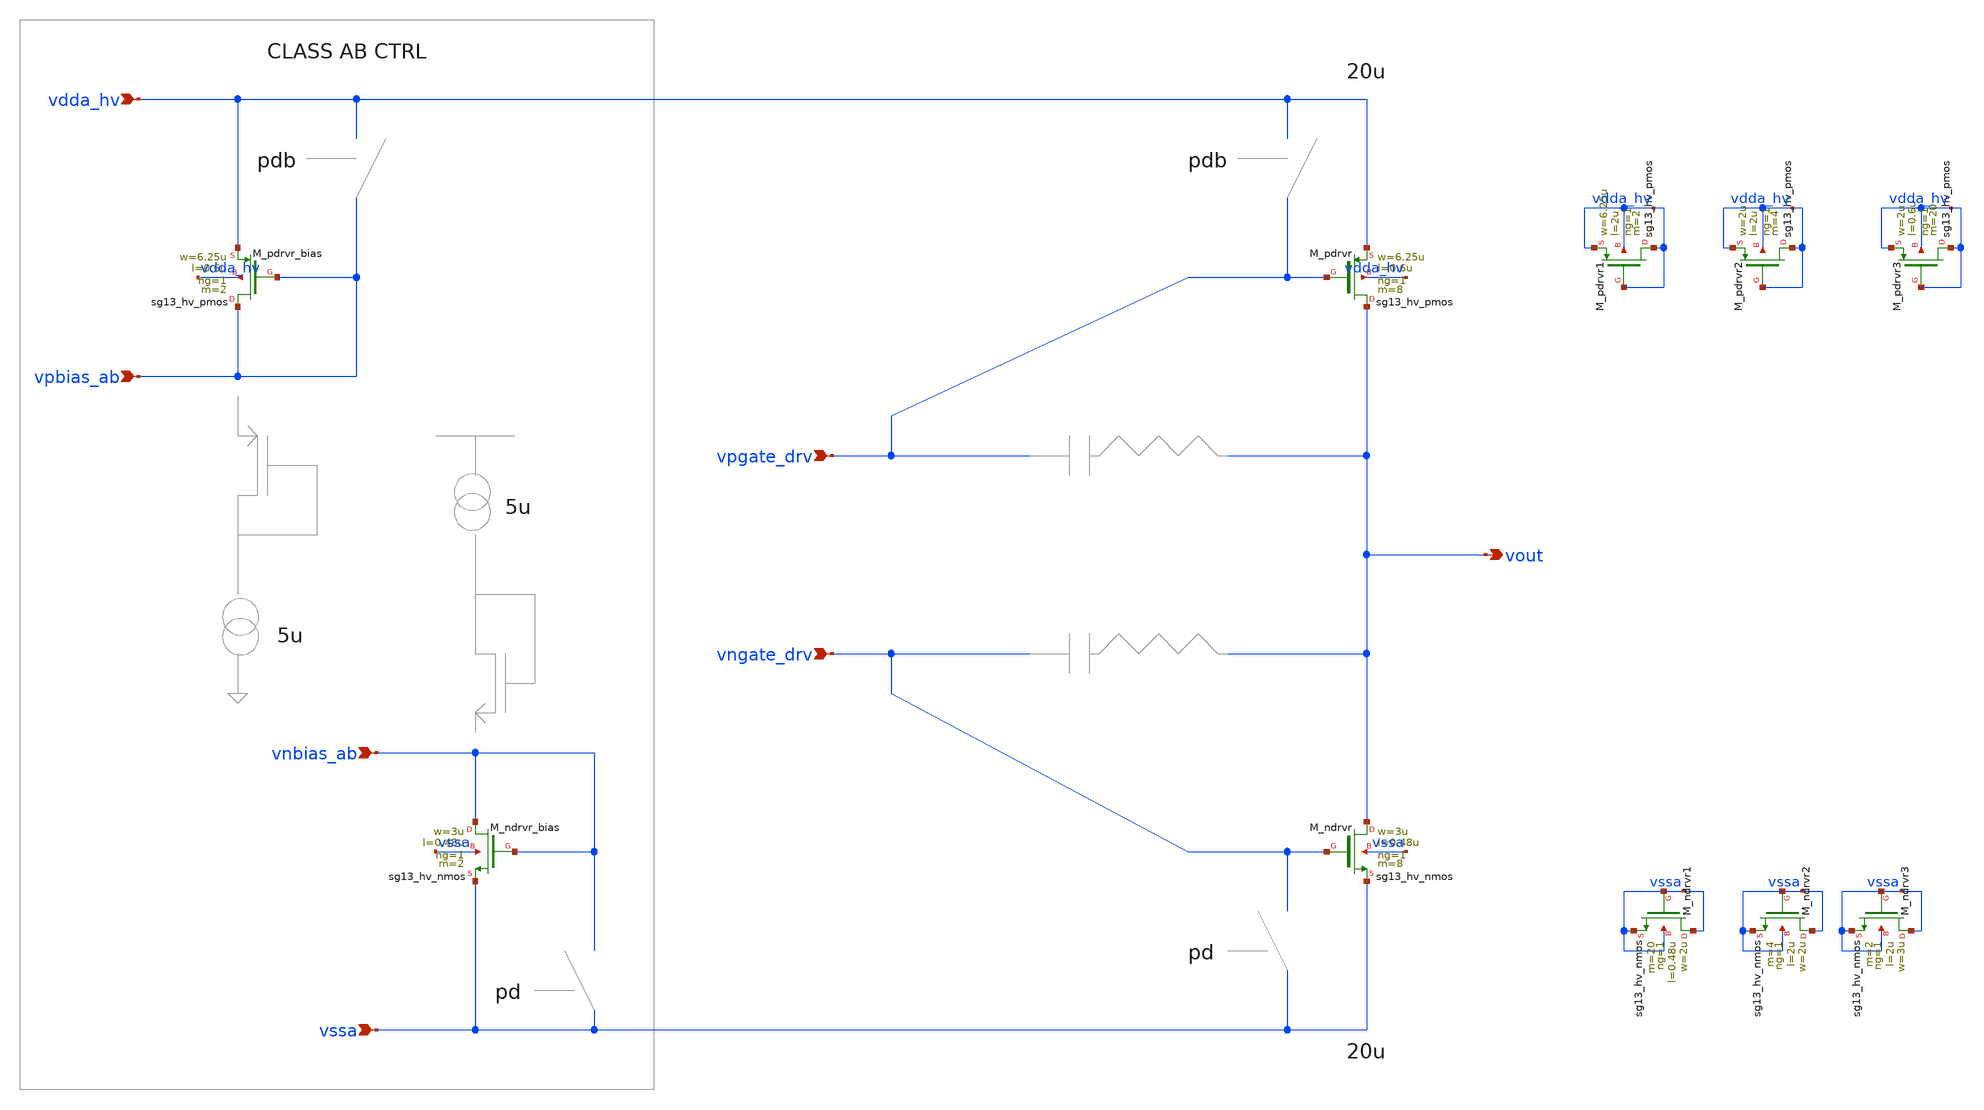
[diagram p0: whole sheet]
** sch_path: Schematics_Layout/sunrise_opamp_stg2_ncomp/sunrise_opamp_stg2_ncomp.sch
**.subckt sunrise_opamp_stg2_ncomp vdda_hv vssa vpgate_drv vngate_drv vout vnbias_ab vpbias_ab
*.ipin vdda_hv
*.ipin vssa
*.ipin vpgate_drv
*.ipin vngate_drv
*.opin vout
*.ipin vnbias_ab
*.ipin vpbias_ab
XM_ndrvr vout vngate_drv vssa vssa sg13_hv_nmos w=3u l=0.48u ng=1 m=8 mm_ok=1
XM_pdrvr vout vpgate_drv vdda_hv vdda_hv sg13_hv_pmos w=6.25u l=0.6u ng=1 m=8 mm_ok=1
XM_pdrvr_bias vpbias_ab vpbias_ab vdda_hv vdda_hv sg13_hv_pmos w=6.25u l=0.6u ng=1 m=2 mm_ok=1
XM_ndrvr_bias vnbias_ab vnbias_ab vssa vssa sg13_hv_nmos w=3u l=0.48u ng=1 m=2 mm_ok=1
XM_pdrvr1 vdda_hv vdda_hv vdda_hv vdda_hv sg13_hv_pmos w=6.25u l=2u ng=1 m=2 mm_ok=1
XM_pdrvr2 vdda_hv vdda_hv vdda_hv vdda_hv sg13_hv_pmos w=2u l=2u ng=1 m=4 mm_ok=1
XM_pdrvr3 vdda_hv vdda_hv vdda_hv vdda_hv sg13_hv_pmos w=2u l=0.6u ng=1 m=20 mm_ok=1
XM_ndrvr1 vssa vssa vssa vssa sg13_hv_nmos w=2u l=0.48u ng=1 m=20 mm_ok=1
XM_ndrvr2 vssa vssa vssa vssa sg13_hv_nmos w=2u l=2u ng=1 m=4 mm_ok=1
XM_ndrvr3 vssa vssa vssa vssa sg13_hv_nmos w=3u l=2u ng=1 m=2 mm_ok=1
**.ends
.end
